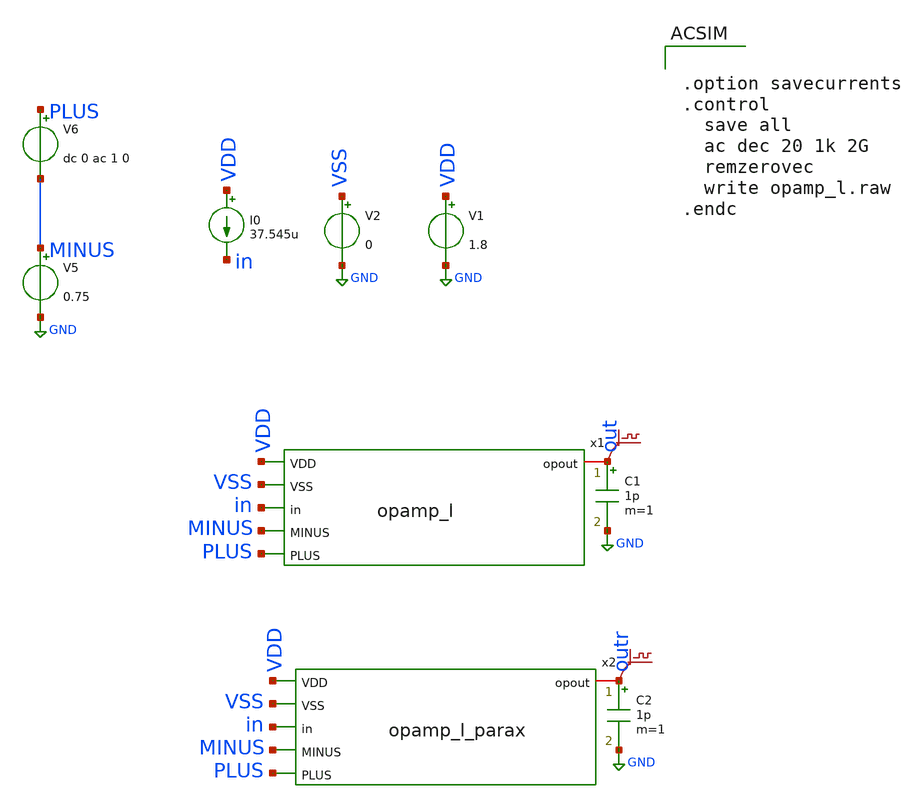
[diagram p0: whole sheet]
** sch_path: custom_gds/tt_um_bgr_agolmanesh/xschem/opamp_l_pl.sch
**.subckt opamp_l_pl
x1 VDD VSS in MINUS PLUS out opamp_l
V1 VDD GND 1.8
V2 VSS GND 0
I0 VDD in 37.545u
V5 MINUS GND 0.75
V6 PLUS MINUS dc 0 ac 1 0
.save v(out)
x2 VDD VSS in MINUS PLUS outr opamp_l_parax
.save v(outr)
C1 out GND 1p m=1
C2 outr GND 1p m=1
**** begin user architecture code

** opencircuitdesign pdks install
.lib $::SKYWATER_MODELS/sky130.lib.spice tt




.option savecurrents
.control
  save all
  ac dec 20 1k 2G
  remzerovec
  write opamp_l.raw
.endc


**** end user architecture code
**.ends

* expanding   symbol:  opamp_l.sym # of pins=6
** sym_path: custom_gds/tt_um_bgr_agolmanesh/xschem/opamp_l.sym
** sch_path: custom_gds/tt_um_bgr_agolmanesh/xschem/opamp_l.sch
.subckt opamp_l VDD VSS in MINUS PLUS opout
*.ipin VDD
*.ipin VSS
*.ipin in
*.ipin MINUS
*.ipin PLUS
*.iopin opout
XM4 opout MINUS net1 VSS sky130_fd_pr__nfet_01v8_lvt L=4 W=16 nf=1 ad='int((nf+1)/2) * W/nf * 0.29' as='int((nf+2)/2) * W/nf * 0.29'
+ pd='2*int((nf+1)/2) * (W/nf + 0.29)' ps='2*int((nf+2)/2) * (W/nf + 0.29)' nrd='0.29 / W' nrs='0.29 / W'
+ sa=0 sb=0 sd=0 mult=1 m=1
XM5 net2 PLUS net1 VSS sky130_fd_pr__nfet_01v8_lvt L=4 W=16 nf=1 ad='int((nf+1)/2) * W/nf * 0.29' as='int((nf+2)/2) * W/nf * 0.29'
+ pd='2*int((nf+1)/2) * (W/nf + 0.29)' ps='2*int((nf+2)/2) * (W/nf + 0.29)' nrd='0.29 / W' nrs='0.29 / W'
+ sa=0 sb=0 sd=0 mult=1 m=1
XM6 opout net2 VDD VDD sky130_fd_pr__pfet_01v8_lvt L=1 W=8 nf=1 ad='int((nf+1)/2) * W/nf * 0.29' as='int((nf+2)/2) * W/nf * 0.29'
+ pd='2*int((nf+1)/2) * (W/nf + 0.29)' ps='2*int((nf+2)/2) * (W/nf + 0.29)' nrd='0.29 / W' nrs='0.29 / W'
+ sa=0 sb=0 sd=0 mult=1 m=1
XM10 net1 in VSS VSS sky130_fd_pr__nfet_01v8_lvt L=0.5 W=4 nf=1 ad='int((nf+1)/2) * W/nf * 0.29' as='int((nf+2)/2) * W/nf * 0.29'
+ pd='2*int((nf+1)/2) * (W/nf + 0.29)' ps='2*int((nf+2)/2) * (W/nf + 0.29)' nrd='0.29 / W' nrs='0.29 / W'
+ sa=0 sb=0 sd=0 mult=1 m=1
XM9 in in VSS VSS sky130_fd_pr__nfet_01v8_lvt L=0.5 W=2 nf=1 ad='int((nf+1)/2) * W/nf * 0.29' as='int((nf+2)/2) * W/nf * 0.29'
+ pd='2*int((nf+1)/2) * (W/nf + 0.29)' ps='2*int((nf+2)/2) * (W/nf + 0.29)' nrd='0.29 / W' nrs='0.29 / W'
+ sa=0 sb=0 sd=0 mult=1 m=1
XM7 net2 net2 VDD VDD sky130_fd_pr__pfet_01v8_lvt L=1 W=8 nf=1 ad='int((nf+1)/2) * W/nf * 0.29' as='int((nf+2)/2) * W/nf * 0.29'
+ pd='2*int((nf+1)/2) * (W/nf + 0.29)' ps='2*int((nf+2)/2) * (W/nf + 0.29)' nrd='0.29 / W' nrs='0.29 / W'
+ sa=0 sb=0 sd=0 mult=1 m=1
.ends


* expanding   symbol:  opamp_l_parax.sym # of pins=6
** sym_path: custom_gds/tt_um_bgr_agolmanesh/xschem/opamp_l.sym
.include [file normalize ../mag/opamp_l.sim.spice]
.GLOBAL GND
.end
